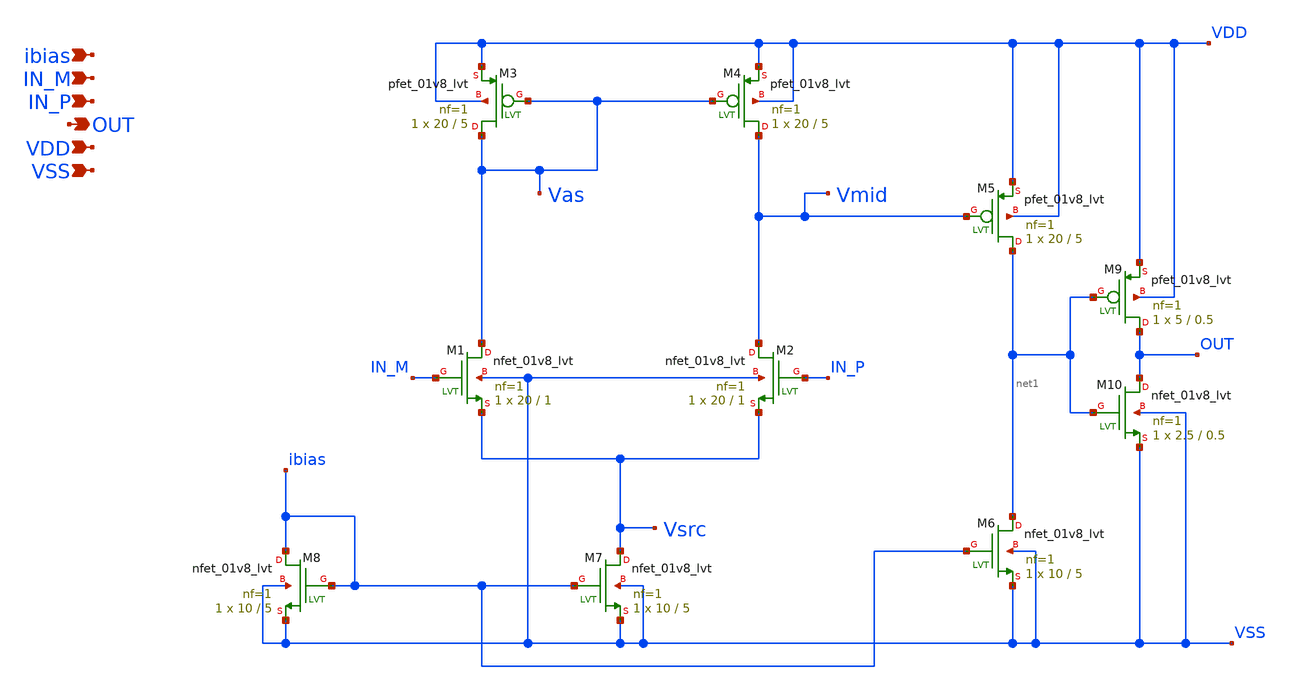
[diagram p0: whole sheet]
** sch_path: xchem/Comparator.sch
**.subckt Comparator IN_M IN_P ibias VDD VSS OUT
*.ipin IN_M
*.ipin IN_P
*.ipin ibias
*.ipin VDD
*.ipin VSS
*.opin OUT
XM4 Vmid Vas VDD VDD sky130_fd_pr__pfet_01v8_lvt L=5 W=20 nf=1 ad='int((nf+1)/2) * W/nf * 0.29' as='int((nf+2)/2) * W/nf * 0.29'
+ pd='2*int((nf+1)/2) * (W/nf + 0.29)' ps='2*int((nf+2)/2) * (W/nf + 0.29)' nrd='0.29 / W' nrs='0.29 / W'
+ sa=0 sb=0 sd=0 mult=1 m=1
XM1 Vas IN_M Vsrc VSS sky130_fd_pr__nfet_01v8_lvt L=1 W=20 nf=1 ad='int((nf+1)/2) * W/nf * 0.29' as='int((nf+2)/2) * W/nf * 0.29'
+ pd='2*int((nf+1)/2) * (W/nf + 0.29)' ps='2*int((nf+2)/2) * (W/nf + 0.29)' nrd='0.29 / W' nrs='0.29 / W'
+ sa=0 sb=0 sd=0 mult=1 m=1
XM2 Vmid IN_P Vsrc VSS sky130_fd_pr__nfet_01v8_lvt L=1 W=20 nf=1 ad='int((nf+1)/2) * W/nf * 0.29' as='int((nf+2)/2) * W/nf * 0.29'
+ pd='2*int((nf+1)/2) * (W/nf + 0.29)' ps='2*int((nf+2)/2) * (W/nf + 0.29)' nrd='0.29 / W' nrs='0.29 / W'
+ sa=0 sb=0 sd=0 mult=1 m=1
XM3 Vas Vas VDD VDD sky130_fd_pr__pfet_01v8_lvt L=5 W=20 nf=1 ad='int((nf+1)/2) * W/nf * 0.29' as='int((nf+2)/2) * W/nf * 0.29'
+ pd='2*int((nf+1)/2) * (W/nf + 0.29)' ps='2*int((nf+2)/2) * (W/nf + 0.29)' nrd='0.29 / W' nrs='0.29 / W'
+ sa=0 sb=0 sd=0 mult=1 m=1
XM5 net1 Vmid VDD VDD sky130_fd_pr__pfet_01v8_lvt L=5 W=20 nf=1 ad='int((nf+1)/2) * W/nf * 0.29' as='int((nf+2)/2) * W/nf * 0.29'
+ pd='2*int((nf+1)/2) * (W/nf + 0.29)' ps='2*int((nf+2)/2) * (W/nf + 0.29)' nrd='0.29 / W' nrs='0.29 / W'
+ sa=0 sb=0 sd=0 mult=1 m=1
XM6 net1 ibias VSS VSS sky130_fd_pr__nfet_01v8_lvt L=5 W=10 nf=1 ad='int((nf+1)/2) * W/nf * 0.29' as='int((nf+2)/2) * W/nf * 0.29'
+ pd='2*int((nf+1)/2) * (W/nf + 0.29)' ps='2*int((nf+2)/2) * (W/nf + 0.29)' nrd='0.29 / W' nrs='0.29 / W'
+ sa=0 sb=0 sd=0 mult=1 m=1
XM7 Vsrc ibias VSS VSS sky130_fd_pr__nfet_01v8_lvt L=5 W=10 nf=1 ad='int((nf+1)/2) * W/nf * 0.29' as='int((nf+2)/2) * W/nf * 0.29'
+ pd='2*int((nf+1)/2) * (W/nf + 0.29)' ps='2*int((nf+2)/2) * (W/nf + 0.29)' nrd='0.29 / W' nrs='0.29 / W'
+ sa=0 sb=0 sd=0 mult=1 m=1
XM8 ibias ibias VSS VSS sky130_fd_pr__nfet_01v8_lvt L=5 W=10 nf=1 ad='int((nf+1)/2) * W/nf * 0.29' as='int((nf+2)/2) * W/nf * 0.29'
+ pd='2*int((nf+1)/2) * (W/nf + 0.29)' ps='2*int((nf+2)/2) * (W/nf + 0.29)' nrd='0.29 / W' nrs='0.29 / W'
+ sa=0 sb=0 sd=0 mult=1 m=1
XM9 OUT net1 VDD VDD sky130_fd_pr__pfet_01v8_lvt L=0.5 W=5 nf=1 ad='int((nf+1)/2) * W/nf * 0.29' as='int((nf+2)/2) * W/nf * 0.29'
+ pd='2*int((nf+1)/2) * (W/nf + 0.29)' ps='2*int((nf+2)/2) * (W/nf + 0.29)' nrd='0.29 / W' nrs='0.29 / W'
+ sa=0 sb=0 sd=0 mult=1 m=1
XM10 OUT net1 VSS VSS sky130_fd_pr__nfet_01v8_lvt L=0.5 W=2.5 nf=1 ad='int((nf+1)/2) * W/nf * 0.29' as='int((nf+2)/2) * W/nf * 0.29'
+ pd='2*int((nf+1)/2) * (W/nf + 0.29)' ps='2*int((nf+2)/2) * (W/nf + 0.29)' nrd='0.29 / W' nrs='0.29 / W'
+ sa=0 sb=0 sd=0 mult=1 m=1
**.ends
.end
